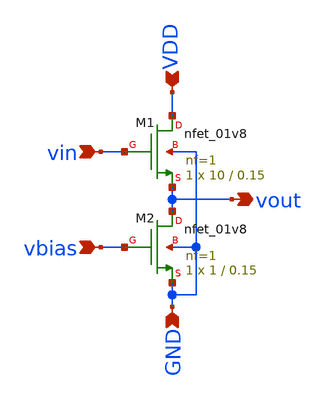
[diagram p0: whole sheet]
** sch_path: schematic/source_follower.sch
**.subckt source_follower GND vin vbias VDD vout
*.ipin GND
*.ipin vin
*.ipin vbias
*.ipin VDD
*.opin vout
XM1 VDD vin vout GND sky130_fd_pr__nfet_01v8 L=0.15 W=10 nf=1 ad='int((nf+1)/2) * W/nf * 0.29' as='int((nf+2)/2) * W/nf * 0.29'
+ pd='2*int((nf+1)/2) * (W/nf + 0.29)' ps='2*int((nf+2)/2) * (W/nf + 0.29)' nrd='0.29 / W' nrs='0.29 / W'
+ sa=0 sb=0 sd=0 mult=1 m=1
XM2 vout vbias GND GND sky130_fd_pr__nfet_01v8 L=0.15 W=1 nf=1 ad='int((nf+1)/2) * W/nf * 0.29' as='int((nf+2)/2) * W/nf * 0.29'
+ pd='2*int((nf+1)/2) * (W/nf + 0.29)' ps='2*int((nf+2)/2) * (W/nf + 0.29)' nrd='0.29 / W' nrs='0.29 / W'
+ sa=0 sb=0 sd=0 mult=1 m=1
**** begin user architecture code

** opencircuitdesign pdks install
.lib $::SKYWATER_MODELS/sky130.lib.spice tt


**** end user architecture code
**.ends
.end
